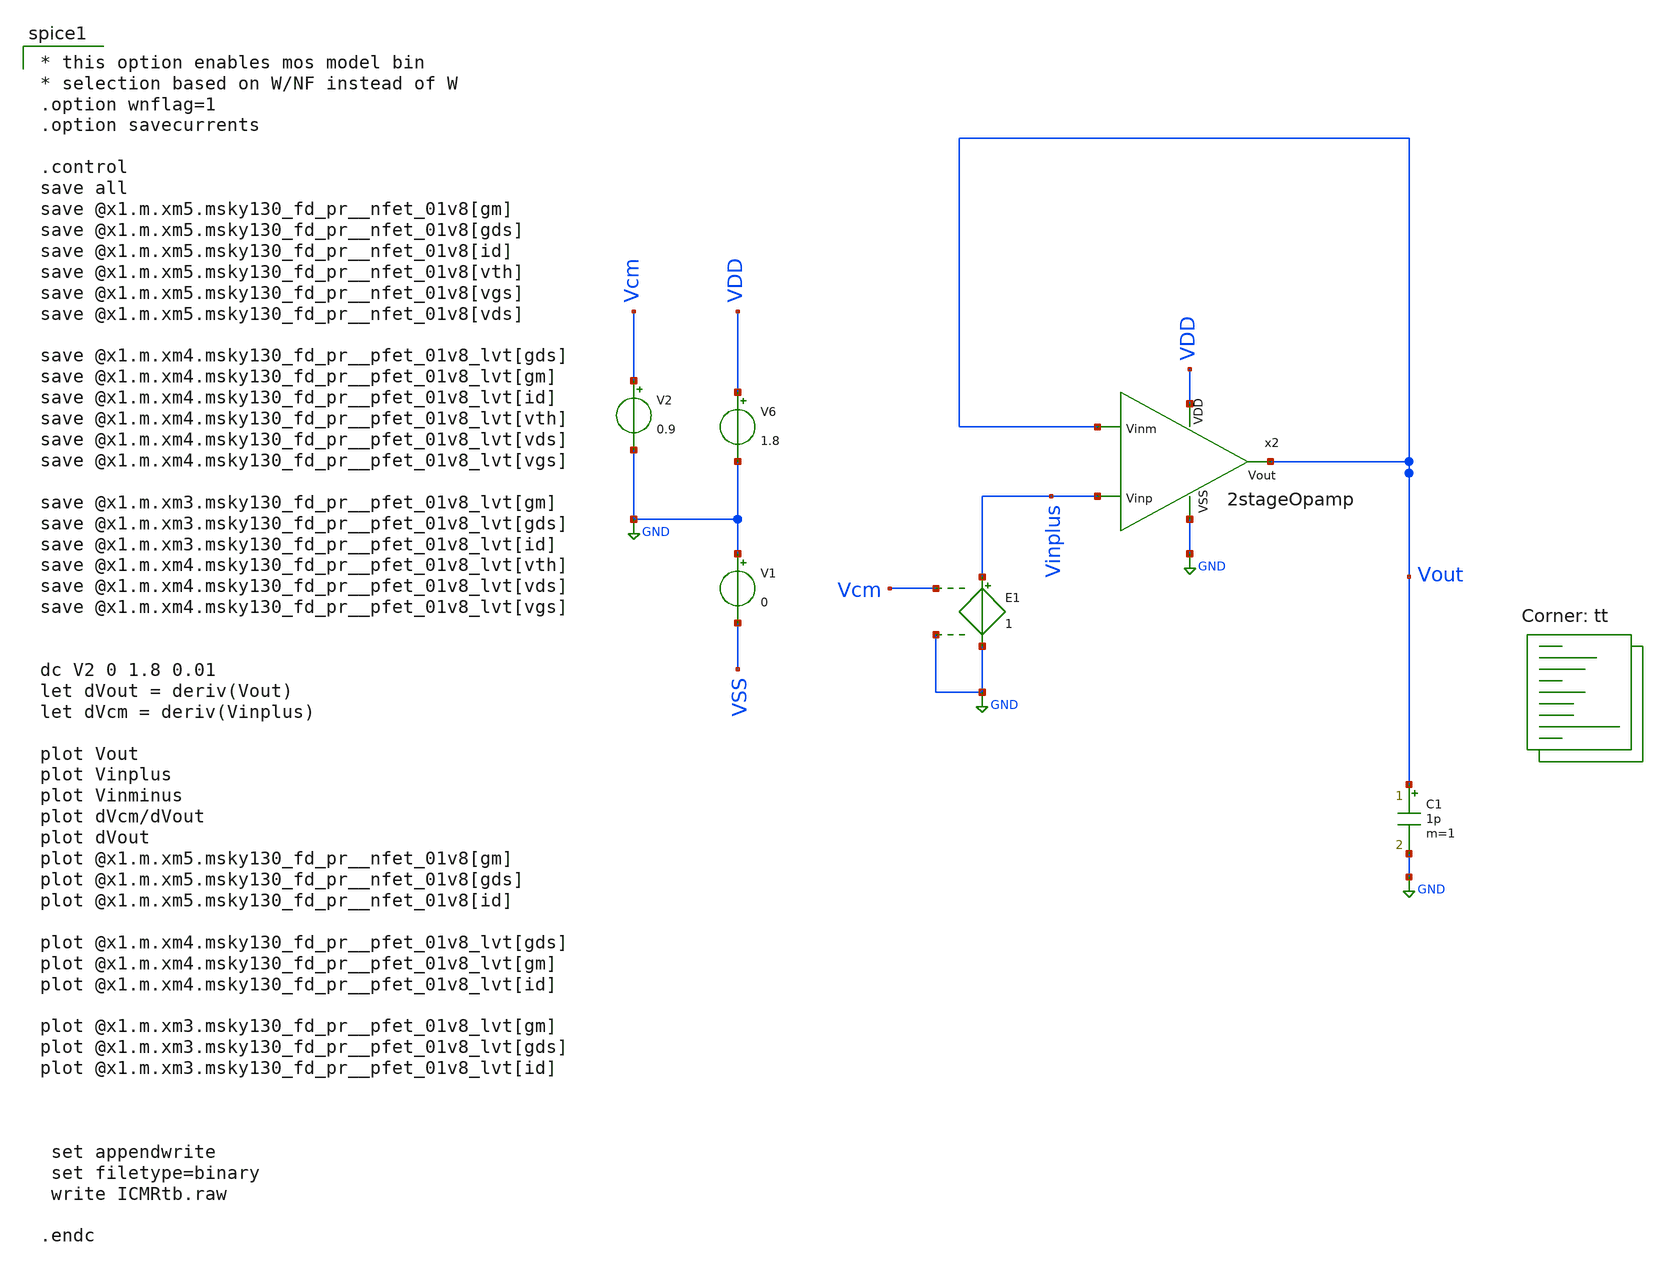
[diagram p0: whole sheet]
** sch_path: xschem/test/xschem/dec24_2stage_tbs/ICMRtb_cp.sch
**.subckt ICMRtb_cp
V2 Vcm GND 0.9
C1 Vout GND 1p m=1
V6 VDD GND 1.8
E1 Vinplus GND Vcm GND 1
V1 GND VSS 0
x2 VDD Vout Vinplus Vout GND 2stageOpamp
**** begin user architecture code
.lib $::SKYWATER_MODELS/sky130.lib.spice tt

* this option enables mos model bin
* selection based on W/NF instead of W
.option wnflag=1
.option savecurrents

.control
save all
save @x1.m.xm5.msky130_fd_pr__nfet_01v8[gm]
save @x1.m.xm5.msky130_fd_pr__nfet_01v8[gds]
save @x1.m.xm5.msky130_fd_pr__nfet_01v8[id]
save @x1.m.xm5.msky130_fd_pr__nfet_01v8[vth]
save @x1.m.xm5.msky130_fd_pr__nfet_01v8[vgs]
save @x1.m.xm5.msky130_fd_pr__nfet_01v8[vds]

save @x1.m.xm4.msky130_fd_pr__pfet_01v8_lvt[gds]
save @x1.m.xm4.msky130_fd_pr__pfet_01v8_lvt[gm]
save @x1.m.xm4.msky130_fd_pr__pfet_01v8_lvt[id]
save @x1.m.xm4.msky130_fd_pr__pfet_01v8_lvt[vth]
save @x1.m.xm4.msky130_fd_pr__pfet_01v8_lvt[vds]
save @x1.m.xm4.msky130_fd_pr__pfet_01v8_lvt[vgs]

save @x1.m.xm3.msky130_fd_pr__pfet_01v8_lvt[gm]
save @x1.m.xm3.msky130_fd_pr__pfet_01v8_lvt[gds]
save @x1.m.xm3.msky130_fd_pr__pfet_01v8_lvt[id]
save @x1.m.xm4.msky130_fd_pr__pfet_01v8_lvt[vth]
save @x1.m.xm4.msky130_fd_pr__pfet_01v8_lvt[vds]
save @x1.m.xm4.msky130_fd_pr__pfet_01v8_lvt[vgs]


dc V2 0 1.8 0.01
let dVout = deriv(Vout)
let dVcm = deriv(Vinplus)

plot Vout
plot Vinplus
plot Vinminus
plot dVcm/dVout
plot dVout
plot @x1.m.xm5.msky130_fd_pr__nfet_01v8[gm]
plot @x1.m.xm5.msky130_fd_pr__nfet_01v8[gds]
plot @x1.m.xm5.msky130_fd_pr__nfet_01v8[id]

plot @x1.m.xm4.msky130_fd_pr__pfet_01v8_lvt[gds]
plot @x1.m.xm4.msky130_fd_pr__pfet_01v8_lvt[gm]
plot @x1.m.xm4.msky130_fd_pr__pfet_01v8_lvt[id]

plot @x1.m.xm3.msky130_fd_pr__pfet_01v8_lvt[gm]
plot @x1.m.xm3.msky130_fd_pr__pfet_01v8_lvt[gds]
plot @x1.m.xm3.msky130_fd_pr__pfet_01v8_lvt[id]



 set appendwrite
 set filetype=binary
 write ICMRtb.raw

.endc


**** end user architecture code
**.ends

* expanding   symbol:  amplifiers/dec24/2stageOpamp.sym # of pins=5
** sym_path: amplifiers/dec24/2stageOpamp.sym
** sch_path: amplifiers/dec24/2stageOpamp.sch
.subckt 2stageOpamp VDD Vinm Vinp Vout VSS
*.ipin Vinm
*.ipin Vinp
*.opin Vout
*.ipin VSS
*.ipin VDD
XM8 Vout net1 VSS VSS sky130_fd_pr__nfet_01v8 L=1 W=6 nf=1 ad='int((nf+1)/2) * W/nf * 0.29' as='int((nf+2)/2) * W/nf * 0.29'
+ pd='2*int((nf+1)/2) * (W/nf + 0.29)' ps='2*int((nf+2)/2) * (W/nf + 0.29)' nrd='0.29 / W' nrs='0.29 / W'
+ sa=0 sb=0 sd=0 mult=8 m=8
XM2 Vout Vb1 VDD VDD sky130_fd_pr__pfet_01v8_lvt L=1 W=9 nf=1 ad='int((nf+1)/2) * W/nf * 0.29' as='int((nf+2)/2) * W/nf * 0.29'
+ pd='2*int((nf+1)/2) * (W/nf + 0.29)' ps='2*int((nf+2)/2) * (W/nf + 0.29)' nrd='0.29 / W' nrs='0.29 / W'
+ sa=0 sb=0 sd=0 mult=3 m=3
XM5 net5 Vb3 net6 VSS sky130_fd_pr__nfet_01v8 L=1 W=4 nf=1 ad='int((nf+1)/2) * W/nf * 0.29' as='int((nf+2)/2) * W/nf * 0.29'
+ pd='2*int((nf+1)/2) * (W/nf + 0.29)' ps='2*int((nf+2)/2) * (W/nf + 0.29)' nrd='0.29 / W' nrs='0.29 / W'
+ sa=0 sb=0 sd=0 mult=3 m=3
XM17 net1 Vb3 net7 VSS sky130_fd_pr__nfet_01v8 L=1 W=4 nf=1 ad='int((nf+1)/2) * W/nf * 0.29' as='int((nf+2)/2) * W/nf * 0.29'
+ pd='2*int((nf+1)/2) * (W/nf + 0.29)' ps='2*int((nf+2)/2) * (W/nf + 0.29)' nrd='0.29 / W' nrs='0.29 / W'
+ sa=0 sb=0 sd=0 mult=3 m=3
XM3 net6 net5 VSS VSS sky130_fd_pr__nfet_01v8 L=1 W=8 nf=1 ad='int((nf+1)/2) * W/nf * 0.29' as='int((nf+2)/2) * W/nf * 0.29'
+ pd='2*int((nf+1)/2) * (W/nf + 0.29)' ps='2*int((nf+2)/2) * (W/nf + 0.29)' nrd='0.29 / W' nrs='0.29 / W'
+ sa=0 sb=0 sd=0 mult=1 m=1
XM19 net7 net5 VSS VSS sky130_fd_pr__nfet_01v8 L=1 W=8 nf=1 ad='int((nf+1)/2) * W/nf * 0.29' as='int((nf+2)/2) * W/nf * 0.29'
+ pd='2*int((nf+1)/2) * (W/nf + 0.29)' ps='2*int((nf+2)/2) * (W/nf + 0.29)' nrd='0.29 / W' nrs='0.29 / W'
+ sa=0 sb=0 sd=0 mult=1 m=1
V1 Vb1 GND 1.1
V2 Vb2 GND 0.7
V3 Vb3 GND 0.9
XM11 net8 Vb1 VDD VDD sky130_fd_pr__pfet_01v8_lvt L=1 W=9 nf=1 ad='int((nf+1)/2) * W/nf * 0.29' as='int((nf+2)/2) * W/nf * 0.29'
+ pd='2*int((nf+1)/2) * (W/nf + 0.29)' ps='2*int((nf+2)/2) * (W/nf + 0.29)' nrd='0.29 / W' nrs='0.29 / W'
+ sa=0 sb=0 sd=0 mult=2 m=2
XM1 net6 Vinm net8 VDD sky130_fd_pr__pfet_01v8_lvt L=1 W=8 nf=1 ad='int((nf+1)/2) * W/nf * 0.29' as='int((nf+2)/2) * W/nf * 0.29'
+ pd='2*int((nf+1)/2) * (W/nf + 0.29)' ps='2*int((nf+2)/2) * (W/nf + 0.29)' nrd='0.29 / W' nrs='0.29 / W'
+ sa=0 sb=0 sd=0 mult=3 m=3
XM15 net7 Vinp net8 VDD sky130_fd_pr__pfet_01v8_lvt L=1 W=8 nf=1 ad='int((nf+1)/2) * W/nf * 0.29' as='int((nf+2)/2) * W/nf * 0.29'
+ pd='2*int((nf+1)/2) * (W/nf + 0.29)' ps='2*int((nf+2)/2) * (W/nf + 0.29)' nrd='0.29 / W' nrs='0.29 / W'
+ sa=0 sb=0 sd=0 mult=3 m=3
XM7 net3 Vb1 VDD VDD sky130_fd_pr__pfet_01v8_lvt L=1 W=9 nf=1 ad='int((nf+1)/2) * W/nf * 0.29' as='int((nf+2)/2) * W/nf * 0.29'
+ pd='2*int((nf+1)/2) * (W/nf + 0.29)' ps='2*int((nf+2)/2) * (W/nf + 0.29)' nrd='0.29 / W' nrs='0.29 / W'
+ sa=0 sb=0 sd=0 mult=1 m=1
XM21 net4 Vb1 VDD VDD sky130_fd_pr__pfet_01v8_lvt L=1 W=9 nf=1 ad='int((nf+1)/2) * W/nf * 0.29' as='int((nf+2)/2) * W/nf * 0.29'
+ pd='2*int((nf+1)/2) * (W/nf + 0.29)' ps='2*int((nf+2)/2) * (W/nf + 0.29)' nrd='0.29 / W' nrs='0.29 / W'
+ sa=0 sb=0 sd=0 mult=1 m=1
XM9 net5 Vb2 net3 VDD sky130_fd_pr__pfet_01v8_lvt L=1 W=9 nf=1 ad='int((nf+1)/2) * W/nf * 0.29' as='int((nf+2)/2) * W/nf * 0.29'
+ pd='2*int((nf+1)/2) * (W/nf + 0.29)' ps='2*int((nf+2)/2) * (W/nf + 0.29)' nrd='0.29 / W' nrs='0.29 / W'
+ sa=0 sb=0 sd=0 mult=1 m=1
XM23 net1 Vb2 net4 VDD sky130_fd_pr__pfet_01v8_lvt L=1 W=9 nf=1 ad='int((nf+1)/2) * W/nf * 0.29' as='int((nf+2)/2) * W/nf * 0.29'
+ pd='2*int((nf+1)/2) * (W/nf + 0.29)' ps='2*int((nf+2)/2) * (W/nf + 0.29)' nrd='0.29 / W' nrs='0.29 / W'
+ sa=0 sb=0 sd=0 mult=1 m=1
XC4 net2 Vout sky130_fd_pr__cap_mim_m3_2 W=7 L=7 MF=4 m=4
R4 net1 net2 7k m=1
.ends

.GLOBAL GND
.end
